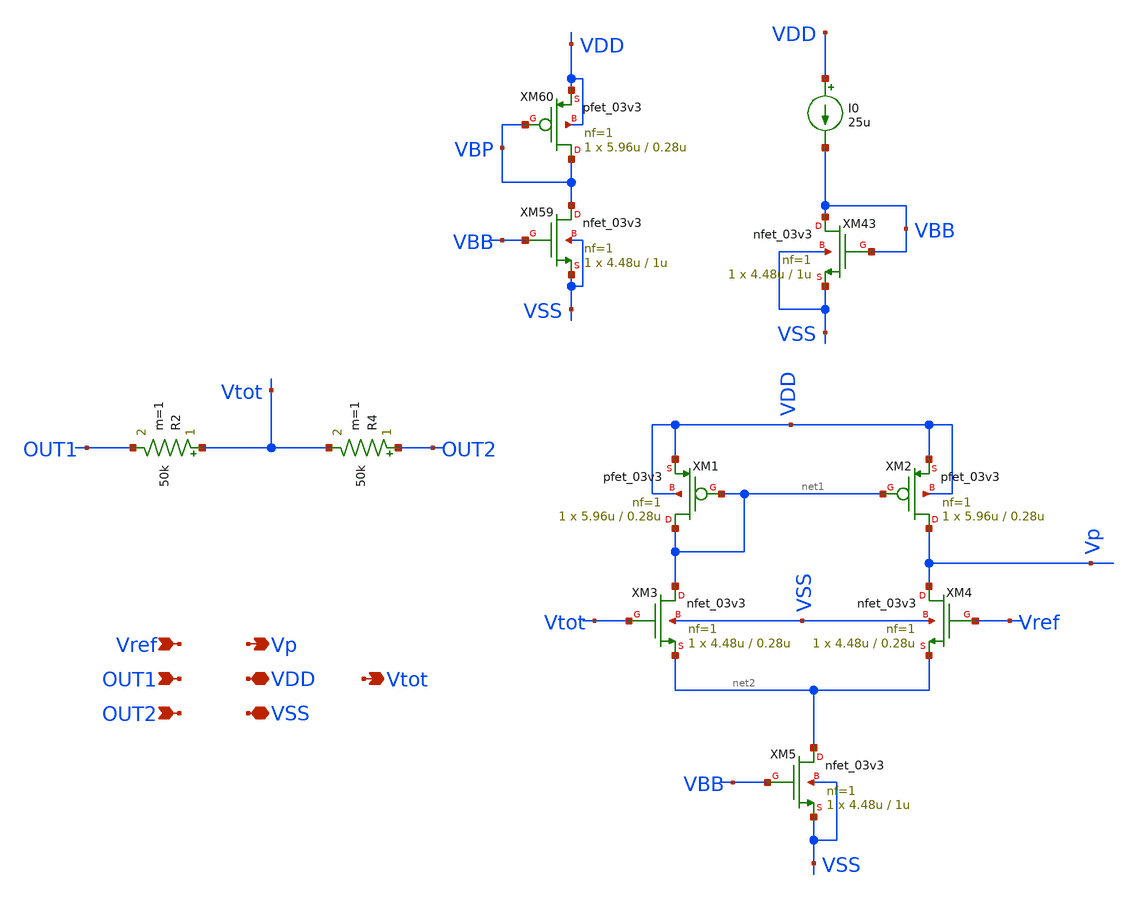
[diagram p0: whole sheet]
** sch_path: SCOP_INPUT_AND_MUX_PAKISTAN_03/Xschem/Others/P_CM_Extraction.sch
**.subckt P_CM_Extraction Vref OUT1 OUT2 Vp VDD VSS Vtot
*.ipin Vref
*.ipin OUT1
*.ipin OUT2
*.opin Vp
*.iopin VDD
*.iopin VSS
*.opin Vtot
R2 Vtot OUT1 50k m=1
R4 OUT2 Vtot 50k m=1
XM59 VBP VBB VSS VSS nfet_03v3 L=1u W=4.48u nf=1 ad='int((nf+1)/2) * W/nf * 0.18u' as='int((nf+2)/2) * W/nf * 0.18u'
+ pd='2*int((nf+1)/2) * (W/nf + 0.18u)' ps='2*int((nf+2)/2) * (W/nf + 0.18u)' nrd='0.18u / W' nrs='0.18u / W'
+ sa=0 sb=0 sd=0 m=1
XM60 VBP VBP VDD VDD pfet_03v3 L=0.28u W=5.96u nf=1 ad='int((nf+1)/2) * W/nf * 0.18u' as='int((nf+2)/2) * W/nf * 0.18u'
+ pd='2*int((nf+1)/2) * (W/nf + 0.18u)' ps='2*int((nf+2)/2) * (W/nf + 0.18u)' nrd='0.18u / W' nrs='0.18u / W'
+ sa=0 sb=0 sd=0 m=1
XM43 VBB VBB VSS VSS nfet_03v3 L=1u W=4.48u nf=1 ad='int((nf+1)/2) * W/nf * 0.18u' as='int((nf+2)/2) * W/nf * 0.18u'
+ pd='2*int((nf+1)/2) * (W/nf + 0.18u)' ps='2*int((nf+2)/2) * (W/nf + 0.18u)' nrd='0.18u / W' nrs='0.18u / W'
+ sa=0 sb=0 sd=0 m=1
I0 VDD VBB 25u
XM1 net1 net1 VDD VDD pfet_03v3 L=0.28u W=5.96u nf=1 ad='int((nf+1)/2) * W/nf * 0.18u' as='int((nf+2)/2) * W/nf * 0.18u'
+ pd='2*int((nf+1)/2) * (W/nf + 0.18u)' ps='2*int((nf+2)/2) * (W/nf + 0.18u)' nrd='0.18u / W' nrs='0.18u / W'
+ sa=0 sb=0 sd=0 m=1
XM2 Vp net1 VDD VDD pfet_03v3 L=0.28u W=5.96u nf=1 ad='int((nf+1)/2) * W/nf * 0.18u' as='int((nf+2)/2) * W/nf * 0.18u'
+ pd='2*int((nf+1)/2) * (W/nf + 0.18u)' ps='2*int((nf+2)/2) * (W/nf + 0.18u)' nrd='0.18u / W' nrs='0.18u / W'
+ sa=0 sb=0 sd=0 m=1
XM3 net1 Vtot net2 VSS nfet_03v3 L=0.28u W=4.48u nf=1 ad='int((nf+1)/2) * W/nf * 0.18u' as='int((nf+2)/2) * W/nf * 0.18u'
+ pd='2*int((nf+1)/2) * (W/nf + 0.18u)' ps='2*int((nf+2)/2) * (W/nf + 0.18u)' nrd='0.18u / W' nrs='0.18u / W'
+ sa=0 sb=0 sd=0 m=1
XM4 Vp Vref net2 VSS nfet_03v3 L=0.28u W=4.48u nf=1 ad='int((nf+1)/2) * W/nf * 0.18u' as='int((nf+2)/2) * W/nf * 0.18u'
+ pd='2*int((nf+1)/2) * (W/nf + 0.18u)' ps='2*int((nf+2)/2) * (W/nf + 0.18u)' nrd='0.18u / W' nrs='0.18u / W'
+ sa=0 sb=0 sd=0 m=1
XM5 net2 VBB VSS VSS nfet_03v3 L=1u W=4.48u nf=1 ad='int((nf+1)/2) * W/nf * 0.18u' as='int((nf+2)/2) * W/nf * 0.18u'
+ pd='2*int((nf+1)/2) * (W/nf + 0.18u)' ps='2*int((nf+2)/2) * (W/nf + 0.18u)' nrd='0.18u / W' nrs='0.18u / W'
+ sa=0 sb=0 sd=0 m=1
**.ends
.end
